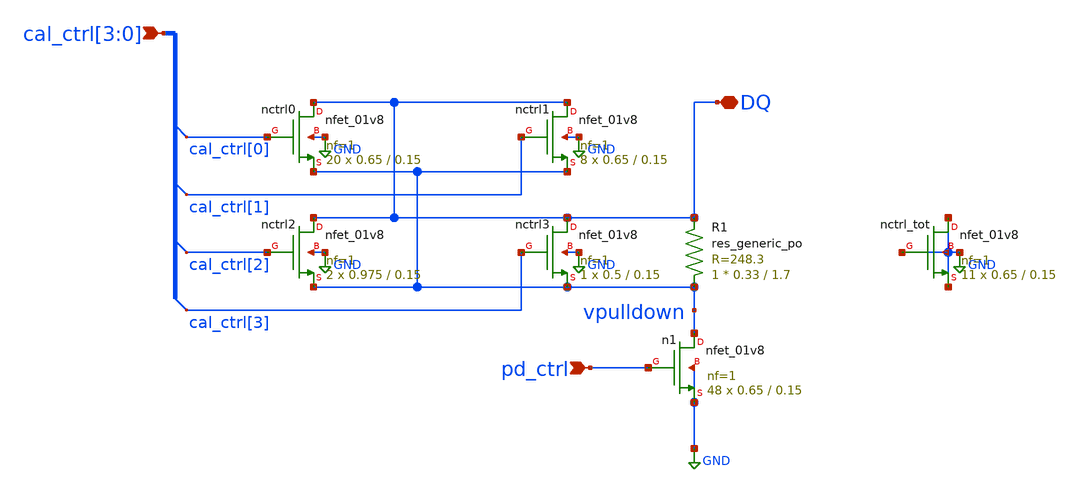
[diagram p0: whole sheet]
** sch_path: n-leg.sch
* Copyright 2021 Stefan Frederik Schippers
* Licensed under the Apache License, Version 2.0 (the "License");
* you may not use this file except in compliance with the License.
* You may obtain a copy of the License at
* https://www.apache.org/licenses/LICENSE-2.0
* Unless required by applicable law or agreed to in writing, software
* distributed under the License is distributed on an "AS IS" BASIS,
* WITHOUT WARRANTIES OR CONDITIONS OF ANY KIND, either express or implied.
* See the License for the specific language governing permissions and
* limitations under the License.
**.subckt n-leg DQ pd_ctrl cal_ctrl[3],cal_ctrl[2],cal_ctrl[1],cal_ctrl[0]
*.iopin DQ
*.ipin pd_ctrl
*.ipin cal_ctrl[3],cal_ctrl[2],cal_ctrl[1],cal_ctrl[0]
XR1 vpulldown DQ sky130_fd_pr__res_generic_po W=0.33 L=1.7 m=1
Xn1 vpulldown pd_ctrl GND GND sky130_fd_pr__nfet_01v8 L=0.15 W=0.65 nf=1 ad='int((nf+1)/2) * W/nf * 0.29'
+ as='int((nf+2)/2) * W/nf * 0.29' pd='2*int((nf+1)/2) * (W/nf + 0.29)' ps='2*int((nf+2)/2) * (W/nf + 0.29)'
+ nrd='0.29 / W' nrs='0.29 / W' sa=0 sb=0 sd=0 mult=48 m=48
Xnctrl0 DQ cal_ctrl[0] vpulldown GND sky130_fd_pr__nfet_01v8 L=0.15 W=0.65 nf=1 ad='int((nf+1)/2) * W/nf * 0.29'
+ as='int((nf+2)/2) * W/nf * 0.29' pd='2*int((nf+1)/2) * (W/nf + 0.29)' ps='2*int((nf+2)/2) * (W/nf + 0.29)'
+ nrd='0.29 / W' nrs='0.29 / W' sa=0 sb=0 sd=0 mult=20 m=20
Xnctrl1 DQ cal_ctrl[1] vpulldown GND sky130_fd_pr__nfet_01v8 L=0.15 W=0.65 nf=1 ad='int((nf+1)/2) * W/nf * 0.29'
+ as='int((nf+2)/2) * W/nf * 0.29' pd='2*int((nf+1)/2) * (W/nf + 0.29)' ps='2*int((nf+2)/2) * (W/nf + 0.29)'
+ nrd='0.29 / W' nrs='0.29 / W' sa=0 sb=0 sd=0 mult=8 m=8
Xnctrl2 DQ cal_ctrl[2] vpulldown GND sky130_fd_pr__nfet_01v8 L=0.15 W=0.975 nf=1 ad='int((nf+1)/2) * W/nf * 0.29'
+ as='int((nf+2)/2) * W/nf * 0.29' pd='2*int((nf+1)/2) * (W/nf + 0.29)' ps='2*int((nf+2)/2) * (W/nf + 0.29)'
+ nrd='0.29 / W' nrs='0.29 / W' sa=0 sb=0 sd=0 mult=2 m=2
Xnctrl3 DQ cal_ctrl[3] vpulldown GND sky130_fd_pr__nfet_01v8 L=0.15 W=0.5 nf=1 ad='int((nf+1)/2) * W/nf * 0.29'
+ as='int((nf+2)/2) * W/nf * 0.29' pd='2*int((nf+1)/2) * (W/nf + 0.29)' ps='2*int((nf+2)/2) * (W/nf + 0.29)'
+ nrd='0.29 / W' nrs='0.29 / W' sa=0 sb=0 sd=0 mult=1 m=1
Xnctrl_tot GND GND GND GND sky130_fd_pr__nfet_01v8 L=0.15 W=0.65 nf=1 ad='int((nf+1)/2) * W/nf * 0.29'
+ as='int((nf+2)/2) * W/nf * 0.29' pd='2*int((nf+1)/2) * (W/nf + 0.29)' ps='2*int((nf+2)/2) * (W/nf + 0.29)'
+ nrd='0.29 / W' nrs='0.29 / W' sa=0 sb=0 sd=0 mult=11 m=11
**.ends
.GLOBAL GND
.end
